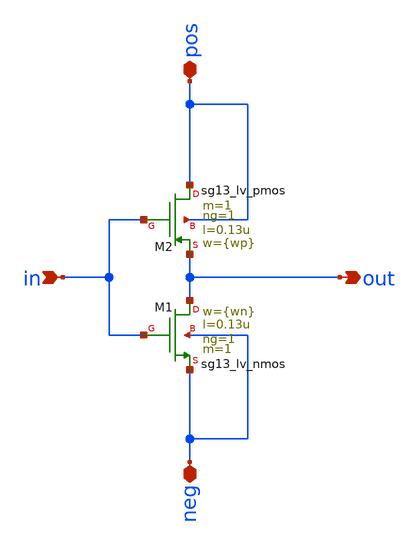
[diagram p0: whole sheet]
** sch_path: TSENSE8490-main/schematic/xschem/analog/inverter/inverter.sch
**.subckt inverter in pos neg out
*.ipin in
*.iopin pos
*.iopin neg
*.opin out
XM1 out in neg neg sg13_lv_nmos w={wn} l=0.13u ng=1 m=1 mm_ok=1
XM2 pos in out pos sg13_lv_pmos w={wp} l=0.13u ng=1 m=1 mm_ok=1
**.ends
.end
